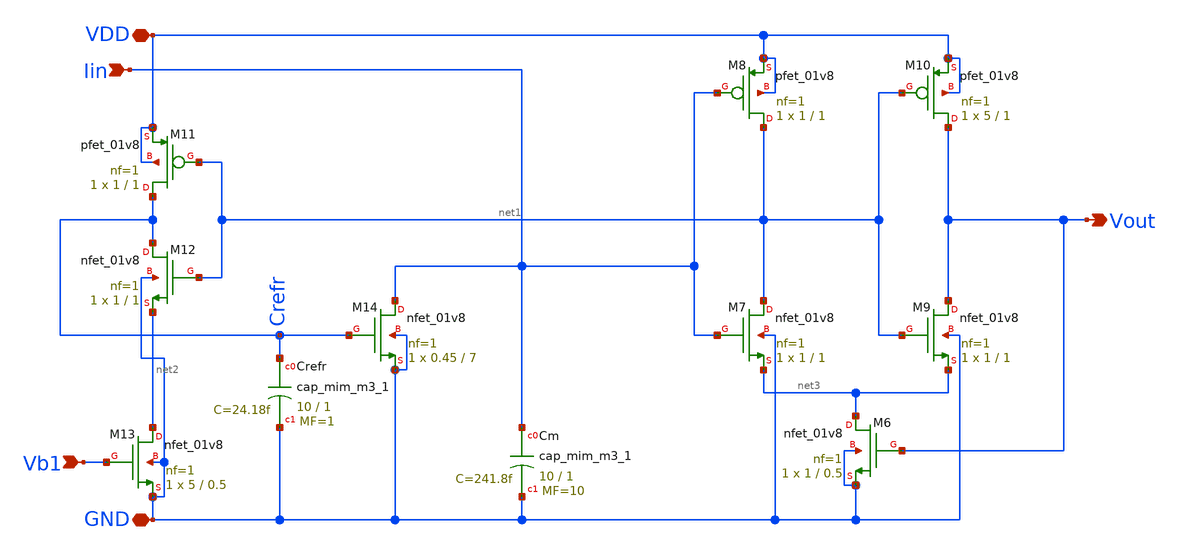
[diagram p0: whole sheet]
** sch_path: LIF_neuron/Presynaptic_LIF_neuron.sch
**.subckt Presynaptic_LIF_neuron GND Vb1 VDD Vout Iin
*.iopin GND
*.ipin Vb1
*.iopin VDD
*.opin Vout
*.ipin Iin
XM13 net2 Vb1 GND GND sky130_fd_pr__nfet_01v8 L=0.5 W=5 nf=1 ad='int((nf+1)/2) * W/nf * 0.29' as='int((nf+2)/2) * W/nf * 0.29'
+ pd='2*int((nf+1)/2) * (W/nf + 0.29)' ps='2*int((nf+2)/2) * (W/nf + 0.29)' nrd='0.29 / W' nrs='0.29 / W'
+ sa=0 sb=0 sd=0 mult=1 m=1
XM12 Crefr net1 net2 GND sky130_fd_pr__nfet_01v8 L=1 W=1 nf=1 ad='int((nf+1)/2) * W/nf * 0.29' as='int((nf+2)/2) * W/nf * 0.29'
+ pd='2*int((nf+1)/2) * (W/nf + 0.29)' ps='2*int((nf+2)/2) * (W/nf + 0.29)' nrd='0.29 / W' nrs='0.29 / W'
+ sa=0 sb=0 sd=0 mult=1 m=1
XM11 Crefr net1 VDD VDD sky130_fd_pr__pfet_01v8 L=1 W=1 nf=1 ad='int((nf+1)/2) * W/nf * 0.29' as='int((nf+2)/2) * W/nf * 0.29'
+ pd='2*int((nf+1)/2) * (W/nf + 0.29)' ps='2*int((nf+2)/2) * (W/nf + 0.29)' nrd='0.29 / W' nrs='0.29 / W'
+ sa=0 sb=0 sd=0 mult=1 m=1
XCrefr Crefr GND sky130_fd_pr__cap_mim_m3_1 W=10 L=1 MF=1 m=1
XM14 Iin Crefr GND GND sky130_fd_pr__nfet_01v8 L=7 W=0.45 nf=1 ad='int((nf+1)/2) * W/nf * 0.29' as='int((nf+2)/2) * W/nf * 0.29'
+ pd='2*int((nf+1)/2) * (W/nf + 0.29)' ps='2*int((nf+2)/2) * (W/nf + 0.29)' nrd='0.29 / W' nrs='0.29 / W'
+ sa=0 sb=0 sd=0 mult=1 m=1
XCm Iin GND sky130_fd_pr__cap_mim_m3_1 W=10 L=1 MF=10 m=10
XM6 net3 Vout GND GND sky130_fd_pr__nfet_01v8 L=0.5 W=1 nf=1 ad='int((nf+1)/2) * W/nf * 0.29' as='int((nf+2)/2) * W/nf * 0.29'
+ pd='2*int((nf+1)/2) * (W/nf + 0.29)' ps='2*int((nf+2)/2) * (W/nf + 0.29)' nrd='0.29 / W' nrs='0.29 / W'
+ sa=0 sb=0 sd=0 mult=1 m=1
XM7 net1 Iin net3 GND sky130_fd_pr__nfet_01v8 L=1 W=1 nf=1 ad='int((nf+1)/2) * W/nf * 0.29' as='int((nf+2)/2) * W/nf * 0.29'
+ pd='2*int((nf+1)/2) * (W/nf + 0.29)' ps='2*int((nf+2)/2) * (W/nf + 0.29)' nrd='0.29 / W' nrs='0.29 / W'
+ sa=0 sb=0 sd=0 mult=1 m=1
XM8 net1 Iin VDD VDD sky130_fd_pr__pfet_01v8 L=1 W=1 nf=1 ad='int((nf+1)/2) * W/nf * 0.29' as='int((nf+2)/2) * W/nf * 0.29'
+ pd='2*int((nf+1)/2) * (W/nf + 0.29)' ps='2*int((nf+2)/2) * (W/nf + 0.29)' nrd='0.29 / W' nrs='0.29 / W'
+ sa=0 sb=0 sd=0 mult=1 m=1
XM9 Vout net1 net3 GND sky130_fd_pr__nfet_01v8 L=1 W=1 nf=1 ad='int((nf+1)/2) * W/nf * 0.29' as='int((nf+2)/2) * W/nf * 0.29'
+ pd='2*int((nf+1)/2) * (W/nf + 0.29)' ps='2*int((nf+2)/2) * (W/nf + 0.29)' nrd='0.29 / W' nrs='0.29 / W'
+ sa=0 sb=0 sd=0 mult=1 m=1
XM10 Vout net1 VDD VDD sky130_fd_pr__pfet_01v8 L=1 W=5 nf=1 ad='int((nf+1)/2) * W/nf * 0.29' as='int((nf+2)/2) * W/nf * 0.29'
+ pd='2*int((nf+1)/2) * (W/nf + 0.29)' ps='2*int((nf+2)/2) * (W/nf + 0.29)' nrd='0.29 / W' nrs='0.29 / W'
+ sa=0 sb=0 sd=0 mult=1 m=1
**.ends
.end
